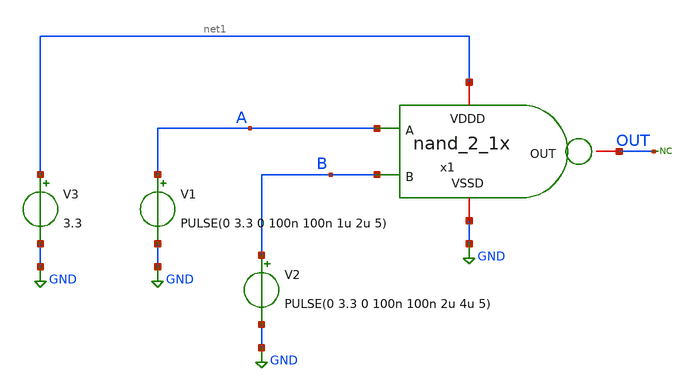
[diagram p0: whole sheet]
** sch_path: SAR_ADC/blocks/SAR_logic/nand_2_1x_tb.sch
**.subckt nand_2_1x_tb
x1 net1 OUT A B GND nand_2_1x
* noconn OUT
V1 A GND PULSE(0 3.3 0 100n 100n 1u 2u 5)
V2 B GND PULSE(0 3.3 0 100n 100n 2u 4u 5)
V3 net1 GND 3.3
**** begin user architecture code



*Parameters
.options TEMPS= 27.0

*Models
.include /home/electrica/Documents/gf180_projects/pdk/gf180mcuC/libs.tech/ngspice/design.ngspice
.lib /home/electrica/Documents/gf180_projects/pdk/gf180mcuC/libs.tech/ngspice/sm141064.ngspice typical
.lib /home/electrica/Documents/gf180_projects/pdk/gf180mcuC/libs.tech/ngspice/smbb000149.ngspice typical


*Data to save
.save all

*Simulation
.control
tran 1n 20u
setplot dc1
plot V(A) V(B) V(OUT)
set filetype=ascii
write nand_2_1x_tb_1.raw

reset
unset filetype
op
save all
write nand_2_1x_tb.raw

.endc
.end



**** end user architecture code
**.ends

* expanding   symbol:
*+  /home/electrica/Documents/gf180_projects/gf180_work/PICO_contest/SAR_logic/nand_2_1x.sym # of pins=5
** sym_path: SAR_ADC/blocks/SAR_logic/nand_2_1x.sym
** sch_path: SAR_ADC/blocks/SAR_logic/nand_2_1x.sch
.subckt nand_2_1x VDDD OUT A B VSSD
*.ipin A
*.ipin B
*.iopin VDDD
*.iopin VSSD
*.iopin OUT
XM1 OUT A VDDD VDDD pfet_03v3 L=0.28u W=0.66u nf=1 ad='int((nf+1)/2) * W/nf * 0.18u' as='int((nf+2)/2) * W/nf * 0.18u'
+ pd='2*int((nf+1)/2) * (W/nf + 0.18u)' ps='2*int((nf+2)/2) * (W/nf + 0.18u)' nrd='0.18u / W' nrs='0.18u / W'
+ sa=0 sb=0 sd=0 m=1 par=1
XM2 OUT B net1 VSSD nfet_03v3 L=0.28u W=0.22u nf=1 ad='int((nf+1)/2) * W/nf * 0.18u' as='int((nf+2)/2) * W/nf * 0.18u'
+ pd='2*int((nf+1)/2) * (W/nf + 0.18u)' ps='2*int((nf+2)/2) * (W/nf + 0.18u)' nrd='0.18u / W' nrs='0.18u / W'
+ sa=0 sb=0 sd=0 m=1 par=1
XM3 OUT B VDDD VDDD pfet_03v3 L=0.28u W=0.66u nf=1 ad='int((nf+1)/2) * W/nf * 0.18u' as='int((nf+2)/2) * W/nf * 0.18u'
+ pd='2*int((nf+1)/2) * (W/nf + 0.18u)' ps='2*int((nf+2)/2) * (W/nf + 0.18u)' nrd='0.18u / W' nrs='0.18u / W'
+ sa=0 sb=0 sd=0 m=1 par=1
XM4 net1 A VSSD VSSD nfet_03v3 L=0.28u W=0.22u nf=1 ad='int((nf+1)/2) * W/nf * 0.18u' as='int((nf+2)/2) * W/nf * 0.18u'
+ pd='2*int((nf+1)/2) * (W/nf + 0.18u)' ps='2*int((nf+2)/2) * (W/nf + 0.18u)' nrd='0.18u / W' nrs='0.18u / W'
+ sa=0 sb=0 sd=0 m=1 par=1
.ends

.GLOBAL GND
.end
